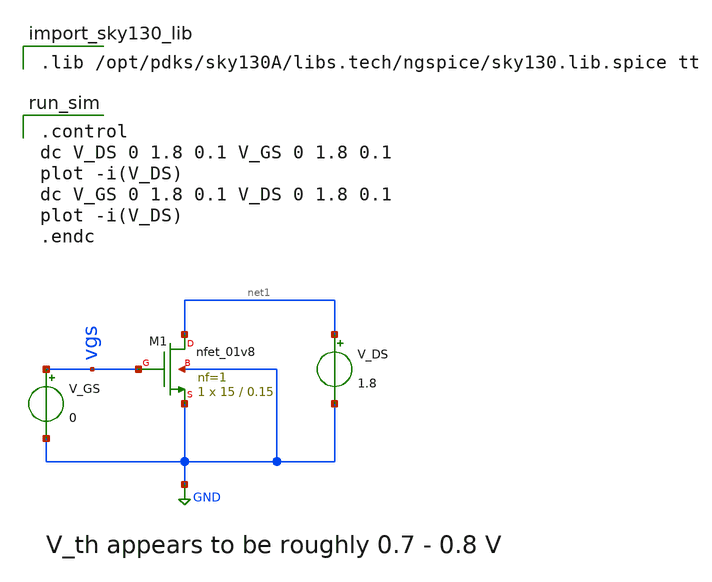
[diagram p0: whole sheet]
** sch_path: xschem/nfet_characterization.sch
**.subckt nfet_characterization
XM1 net1 vgs GND GND sky130_fd_pr__nfet_01v8 L=0.15 W=15 nf=1 ad='int((nf+1)/2) * W/nf * 0.29' as='int((nf+2)/2) * W/nf * 0.29'
+ pd='2*int((nf+1)/2) * (W/nf + 0.29)' ps='2*int((nf+2)/2) * (W/nf + 0.29)' nrd='0.29 / W' nrs='0.29 / W'
+ sa=0 sb=0 sd=0 mult=1 m=1
V_GS vgs GND 0
V_DS net1 GND 1.8
**** begin user architecture code

.lib /opt/pdks/sky130A/libs.tech/ngspice/sky130.lib.spice tt


.control
dc V_DS 0 1.8 0.1 V_GS 0 1.8 0.1
plot -i(V_DS)
dc V_GS 0 1.8 0.1 V_DS 0 1.8 0.1
plot -i(V_DS)
.endc

**** end user architecture code
**.ends
.GLOBAL GND
.end
